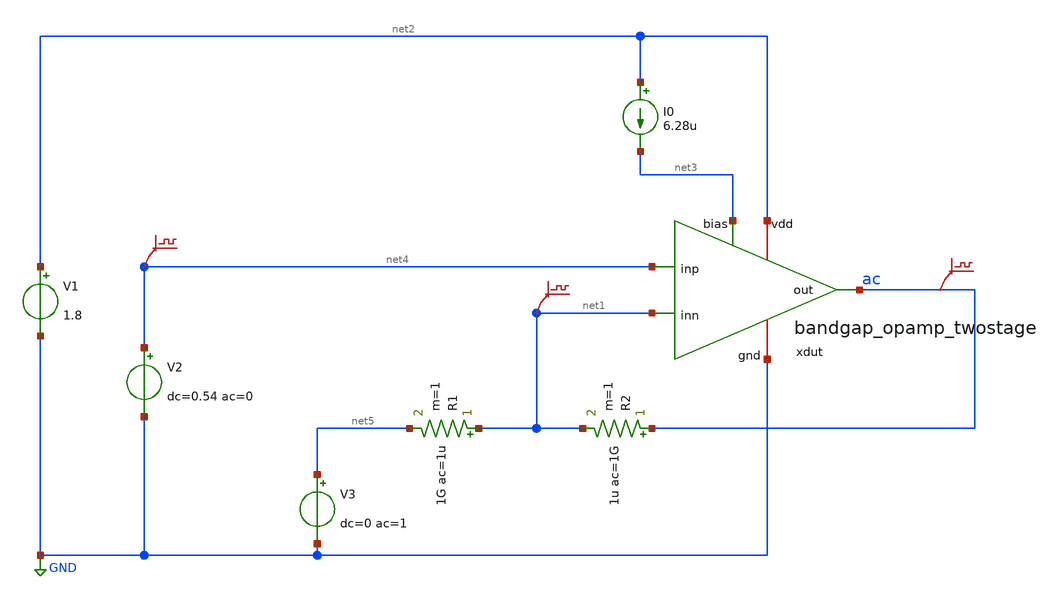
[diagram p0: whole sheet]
** sch_path: design/bandgap_opamp_twostage/test/bandgap_opamp_test.sch
**.subckt bandgap_opamp_test
V1 net2 GND 1.8
xdut net2 ac net4 net1 net3 GND bandgap_opamp_twostage
I0 net2 net3 6.28u
V2 net4 GND dc=0.54 ac=0
V3 net5 GND dc=0 ac=1
R1 net1 net5 1G ac=1u m=1
R2 ac net1 1u ac=1G m=1
.save v(ac)
.save v(net4)
.save v(net1)
**** begin user architecture code


*.include sky130_fd_pr/models/corners/tt.spice
.lib sky130_fd_pr/models/sky130.lib.spice tt



.temp 125

*.save @M.X1.XMdiff.msky130_fd_pr__pfet_01v8_lvt[vdsat] @M.X1.XMfold.msky130_fd_pr__nfet_01v8_lvt[vdsat] @M.X1.XMcas.msky130_fd_pr__nfet_01v8_lvt[vdsat] @M.X1.XMload.msky130_fd_pr__pfet_01v8_lvt[vdsat] @M.X1.XMdiffcurr.msky130_fd_pr__pfet_01v8_lvt[vdsat]

.save all @M.xdut.xmmnr.msky130_fd_pr__nfet_01v8_lvt[vdsat] @M.xdut.xmmpr.msky130_fd_pr__pfet_01v8_lvt[vdsat] @M.xdut.xmcasn.msky130_fd_pr__nfet_01v8_lvt[gm] @M.xdut.xmcasn.msky130_fd_pr__nfet_01v8_lvt[vdsat] @M.xdut.xmloadmp.msky130_fd_pr__pfet_01v8_lvt[vdsat] @M.xdut.xmdiffn.msky130_fd_pr__pfet_01v8_lvt[gm] @M.xdut.xmgain.msky130_fd_pr__pfet_01v8_lvt[vdsat] @M.xdut.xmgain.msky130_fd_pr__pfet_01v8_lvt[gm] @M.xdut.xmcas_foldn.msky130_fd_pr__nfet_01v8_lvt[vdsat] @M.xdut.xmcurr_foldn.msky130_fd_pr__nfet_01v8_lvt[vdsat] @M.xdut.xmdiffn.msky130_fd_pr__pfet_01v8_lvt[vdsat] @M.xdut.xmloadcp.msky130_fd_pr__pfet_01v8_lvt[vdsat] @M.xdut.xmloadmp.msky130_fd_pr__pfet_01v8_lvt[vdsat]

.op
.ac dec 10 1 1000Meg

*.tf v(ac) V3

*.dc temp -40 125 1.65

.option savecurrents

.control
  run
  setplot ac1
  set units=degrees
  gnuplot bandgap_opamp_test db(ac) ph(ac)
.endc


**** end user architecture code
**.ends

* expanding   symbol:  bandgap_opamp_twostage/bandgap_opamp_twostage.sym # of pins=6
** sym_path: design/bandgap_opamp_twostage/bandgap_opamp_twostage.sym
** sch_path: design/bandgap_opamp_twostage/bandgap_opamp_twostage.sch
.subckt bandgap_opamp_twostage vdd out inp inn bias gnd
*.ipin inp
*.ipin inn
*.ipin bias
*.opin out
*.iopin vdd
*.iopin gnd
XMmpdiff net8 net5 vdd vdd sky130_fd_pr__pfet_01v8_lvt L=8 W=5 nf=1 ad='W * 0.29' as='W * 0.29' pd='2 * (W + 0.29)'
+ ps='2 * (W + 0.29)' nrd='0.29 / W' nrs='0.29 / W' sa=0 sb=0 sd=0 mult=16 m=16
XMmpr net5 net5 vdd vdd sky130_fd_pr__pfet_01v8_lvt L=8 W=5 nf=1 ad='W * 0.29' as='W * 0.29' pd='2 * (W + 0.29)'
+ ps='2 * (W + 0.29)' nrd='0.29 / W' nrs='0.29 / W' sa=0 sb=0 sd=0 mult=4 m=4
XMmnr bias bias gnd gnd sky130_fd_pr__nfet_01v8_lvt L=4 W=2 nf=1 ad='W * 0.29' as='W * 0.29' pd='2 * (W + 0.29)'
+ ps='2 * (W + 0.29)' nrd='0.29 / W' nrs='0.29 / W' sa=0 sb=0 sd=0 mult=8 m=8
XMmnb net5 bias gnd gnd sky130_fd_pr__nfet_01v8_lvt L=4 W=2 nf=1 ad='W * 0.29' as='W * 0.29' pd='2 * (W + 0.29)'
+ ps='2 * (W + 0.29)' nrd='0.29 / W' nrs='0.29 / W' sa=0 sb=0 sd=0 mult=2 m=2
XMtrioden net11 net3 gnd gnd sky130_fd_pr__nfet_01v8_lvt L=8 W=1 nf=1 ad='W * 0.29' as='W * 0.29' pd='2 * (W + 0.29)'
+ ps='2 * (W + 0.29)' nrd='0.29 / W' nrs='0.29 / W' sa=0 sb=0 sd=0 mult=2 m=2
XMmpa net10 net5 vdd vdd sky130_fd_pr__pfet_01v8_lvt L=8 W=5 nf=1 ad='W * 0.29' as='W * 0.29' pd='2 * (W + 0.29)'
+ ps='2 * (W + 0.29)' nrd='0.29 / W' nrs='0.29 / W' sa=0 sb=0 sd=0 mult=4 m=4
XMcpdiff net1 net9 net8 vdd sky130_fd_pr__pfet_01v8_lvt L=0.5 W=5 nf=1 ad='W * 0.29' as='W * 0.29' pd='2 * (W + 0.29)'
+ ps='2 * (W + 0.29)' nrd='0.29 / W' nrs='0.29 / W' sa=0 sb=0 sd=0 mult=16 m=16
XMmna net9 bias gnd gnd sky130_fd_pr__nfet_01v8_lvt L=4 W=2 nf=1 ad='W * 0.29' as='W * 0.29' pd='2 * (W + 0.29)'
+ ps='2 * (W + 0.29)' nrd='0.29 / W' nrs='0.29 / W' sa=0 sb=0 sd=0 mult=2 m=2
XMtriodep net12 net9 vdd vdd sky130_fd_pr__pfet_01v8_lvt L=8 W=5 nf=1 ad='W * 0.29' as='W * 0.29' pd='2 * (W + 0.29)'
+ ps='2 * (W + 0.29)' nrd='0.29 / W' nrs='0.29 / W' sa=0 sb=0 sd=0 mult=4 m=4
XMcpa net3 net9 net10 vdd sky130_fd_pr__pfet_01v8_lvt L=0.5 W=5 nf=1 ad='W * 0.29' as='W * 0.29' pd='2 * (W + 0.29)'
+ ps='2 * (W + 0.29)' nrd='0.29 / W' nrs='0.29 / W' sa=0 sb=0 sd=0 mult=2 m=2
XMcasba net3 net3 net11 gnd sky130_fd_pr__nfet_01v8_lvt L=5 W=7 nf=1 ad='W * 0.29' as='W * 0.29' pd='2 * (W + 0.29)'
+ ps='2 * (W + 0.29)' nrd='0.29 / W' nrs='0.29 / W' sa=0 sb=0 sd=0 mult=32 m=32
.save v(net2)
XMcasn out net3 net6 gnd sky130_fd_pr__nfet_01v8_lvt L=0.35 W=7 nf=1 ad='W * 0.29' as='W * 0.29' pd='2 * (W + 0.29)'
+ ps='2 * (W + 0.29)' nrd='0.29 / W' nrs='0.29 / W' sa=0 sb=0 sd=0 mult=32 m=32
XMcasp net4 net3 net2 gnd sky130_fd_pr__nfet_01v8_lvt L=0.35 W=7 nf=1 ad='W * 0.29' as='W * 0.29' pd='2 * (W + 0.29)'
+ ps='2 * (W + 0.29)' nrd='0.29 / W' nrs='0.29 / W' sa=0 sb=0 sd=0 mult=32 m=32
XMload_mp net14 net4 vdd vdd sky130_fd_pr__pfet_01v8_lvt L=8 W=5 nf=1 ad='W * 0.29' as='W * 0.29' pd='2 * (W + 0.29)'
+ ps='2 * (W + 0.29)' nrd='0.29 / W' nrs='0.29 / W' sa=0 sb=0 sd=0 mult=8 m=8
XMload_mn net15 net4 vdd vdd sky130_fd_pr__pfet_01v8_lvt L=8 W=5 nf=1 ad='W * 0.29' as='W * 0.29' pd='2 * (W + 0.29)'
+ ps='2 * (W + 0.29)' nrd='0.29 / W' nrs='0.29 / W' sa=0 sb=0 sd=0 mult=8 m=8
XMloadcn out net7 net15 vdd sky130_fd_pr__pfet_01v8_lvt L=0.35 W=5 nf=1 ad='W * 0.29' as='W * 0.29' pd='2 * (W + 0.29)'
+ ps='2 * (W + 0.29)' nrd='0.29 / W' nrs='0.29 / W' sa=0 sb=0 sd=0 mult=8 m=8
XMloadcp net4 net7 net14 vdd sky130_fd_pr__pfet_01v8_lvt L=0.35 W=5 nf=1 ad='W * 0.29' as='W * 0.29'
+ pd='2 * (W + 0.29)' ps='2 * (W + 0.29)' nrd='0.29 / W' nrs='0.29 / W' sa=0 sb=0 sd=0 mult=8 m=8
XMcurr_foldn net16 bias gnd gnd sky130_fd_pr__nfet_01v8_lvt L=4 W=2 nf=1 ad='W * 0.29' as='W * 0.29'
+ pd='2 * (W + 0.29)' ps='2 * (W + 0.29)' nrd='0.29 / W' nrs='0.29 / W' sa=0 sb=0 sd=0 mult=8 m=8
XMcurr_foldp net17 bias gnd gnd sky130_fd_pr__nfet_01v8_lvt L=4 W=2 nf=1 ad='W * 0.29' as='W * 0.29'
+ pd='2 * (W + 0.29)' ps='2 * (W + 0.29)' nrd='0.29 / W' nrs='0.29 / W' sa=0 sb=0 sd=0 mult=8 m=8
XMdiffn net6 inn net1 net1 sky130_fd_pr__pfet_01v8_lvt L=5 W=7 nf=1 ad='W * 0.29' as='W * 0.29' pd='2 * (W + 0.29)'
+ ps='2 * (W + 0.29)' nrd='0.29 / W' nrs='0.29 / W' sa=0 sb=0 sd=0 mult=256 m=256
XMdiffp net2 inp net1 net1 sky130_fd_pr__pfet_01v8_lvt L=5 W=7 nf=1 ad='W * 0.29' as='W * 0.29' pd='2 * (W + 0.29)'
+ ps='2 * (W + 0.29)' nrd='0.29 / W' nrs='0.29 / W' sa=0 sb=0 sd=0 mult=256 m=256
.save v(net3)
.save v(net1)
.save v(net21)
.save v(net22)
.save v(net15)
.save v(net4)
XMcpdiff1 net9 net9 net12 vdd sky130_fd_pr__pfet_01v8_lvt L=0.5 W=5 nf=1 ad='W * 0.29' as='W * 0.29'
+ pd='2 * (W + 0.29)' ps='2 * (W + 0.29)' nrd='0.29 / W' nrs='0.29 / W' sa=0 sb=0 sd=0 mult=2 m=2
.save v(net6)
XMtriode_rload net13 net7 vdd vdd sky130_fd_pr__pfet_01v8_lvt L=1 W=5 nf=1 ad='W * 0.29' as='W * 0.29'
+ pd='2 * (W + 0.29)' ps='2 * (W + 0.29)' nrd='0.29 / W' nrs='0.29 / W' sa=0 sb=0 sd=0 mult=4 m=4
XMcas_rload net7 net7 net13 vdd sky130_fd_pr__pfet_01v8_lvt L=0.35 W=5 nf=1 ad='W * 0.29' as='W * 0.29'
+ pd='2 * (W + 0.29)' ps='2 * (W + 0.29)' nrd='0.29 / W' nrs='0.29 / W' sa=0 sb=0 sd=0 mult=1 m=1
XMmnc net7 bias gnd gnd sky130_fd_pr__nfet_01v8_lvt L=4 W=2 nf=1 ad='W * 0.29' as='W * 0.29' pd='2 * (W + 0.29)'
+ ps='2 * (W + 0.29)' nrd='0.29 / W' nrs='0.29 / W' sa=0 sb=0 sd=0 mult=1 m=1
XMcas_foldn net6 net18 net16 gnd sky130_fd_pr__nfet_01v8_lvt L=0.35 W=2 nf=1 ad='W * 0.29' as='W * 0.29'
+ pd='2 * (W + 0.29)' ps='2 * (W + 0.29)' nrd='0.29 / W' nrs='0.29 / W' sa=0 sb=0 sd=0 mult=8 m=8
XMcas_foldp net2 net18 net17 gnd sky130_fd_pr__nfet_01v8_lvt L=0.35 W=2 nf=1 ad='W * 0.29' as='W * 0.29'
+ pd='2 * (W + 0.29)' ps='2 * (W + 0.29)' nrd='0.29 / W' nrs='0.29 / W' sa=0 sb=0 sd=0 mult=8 m=8
XMmfn3 net18 net18 net19 gnd sky130_fd_pr__nfet_01v8_lvt L=0.35 W=2 nf=1 ad='W * 0.29' as='W * 0.29'
+ pd='2 * (W + 0.29)' ps='2 * (W + 0.29)' nrd='0.29 / W' nrs='0.29 / W' sa=0 sb=0 sd=0 mult=8 m=8
XMtriode_ncas net19 net18 gnd gnd sky130_fd_pr__nfet_01v8_lvt L=4 W=2 nf=1 ad='W * 0.29' as='W * 0.29'
+ pd='2 * (W + 0.29)' ps='2 * (W + 0.29)' nrd='0.29 / W' nrs='0.29 / W' sa=0 sb=0 sd=0 mult=1 m=1
XMmpdiff1 net20 net5 vdd vdd sky130_fd_pr__pfet_01v8_lvt L=8 W=5 nf=1 ad='W * 0.29' as='W * 0.29' pd='2 * (W + 0.29)'
+ ps='2 * (W + 0.29)' nrd='0.29 / W' nrs='0.29 / W' sa=0 sb=0 sd=0 mult=8 m=8
XMcpdiff2 net18 net9 net20 vdd sky130_fd_pr__pfet_01v8_lvt L=0.5 W=5 nf=1 ad='W * 0.29' as='W * 0.29'
+ pd='2 * (W + 0.29)' ps='2 * (W + 0.29)' nrd='0.29 / W' nrs='0.29 / W' sa=0 sb=0 sd=0 mult=8 m=8
.save v(net18)
.save v(net16)
.save v(net4)
C1 net14 out 30p m=1
.save v(net14)
.ends

.GLOBAL GND
.end
